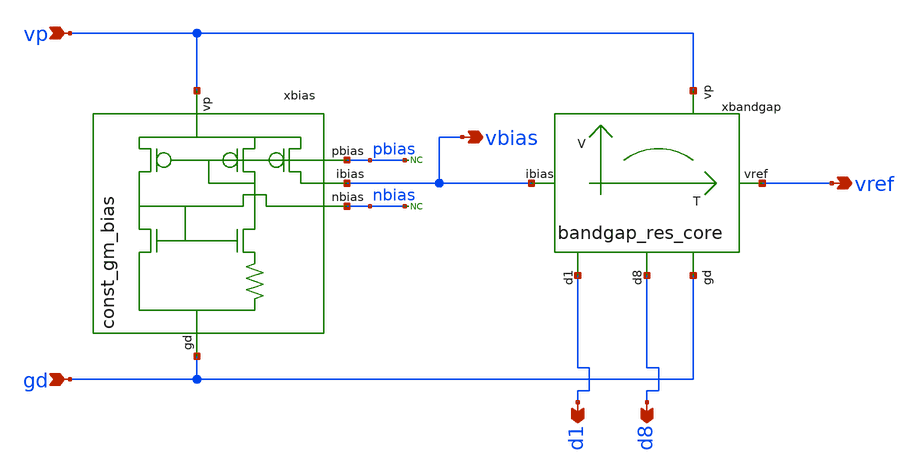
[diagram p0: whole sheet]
** sch_path: PLL0663-main/schematic/xschem/bandgap/bandgap_res_core_wrapper.sch
**.subckt bandgap_res_core_wrapper vp gd vref d1 d8 vbias
*.ipin vp
*.ipin gd
*.opin vref
*.opin d1
*.opin d8
*.opin vbias
xbandgap vp vbias vref gd d8 d1 bandgap_res_core
xbias vp vbias gd pbias nbias const_gm_bias
* noconn nbias
* noconn pbias
**.ends
.end
